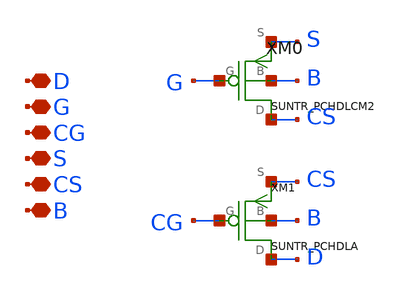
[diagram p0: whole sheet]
** sch_path: ip/sun_tr_sky130nm/design/SUN_TR_SKY130NM/SUNTR_CPCHDLCM2.sch
**.subckt SUNTR_CPCHDLCM2 D G CG S CS B
*.iopin D
*.iopin G
*.iopin CG
*.iopin S
*.iopin CS
*.iopin B
XM0 G CS B S SUNTR_PCHDLCM2
XM1 D CG CS B SUNTR_PCHDLA xoffset=0 yoffset=0 angle=0
**.ends
.end
